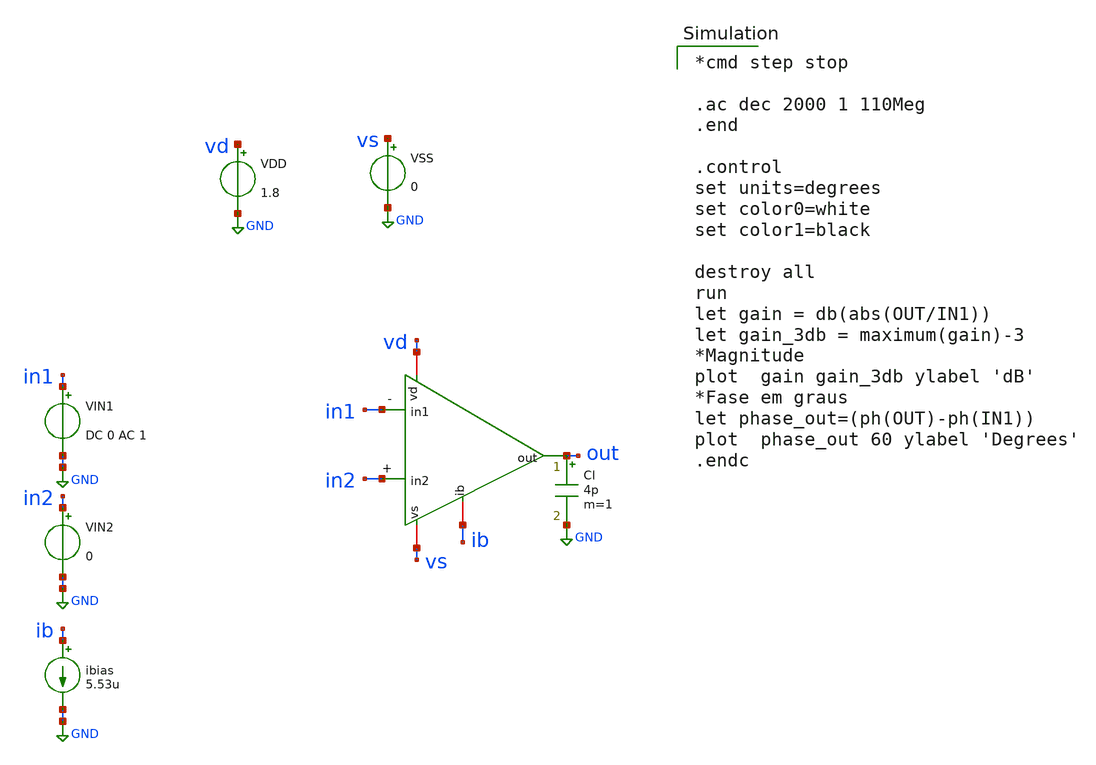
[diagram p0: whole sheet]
** sch_path: amp-op/xschem/ampop_tb-ac.sch
* Copyright 2020 Stefan Frederik Schippers
* Licensed under the Apache License, Version 2.0 (the "License");
* you may not use this file except in compliance with the License.
* You may obtain a copy of the License at
* https://www.apache.org/licenses/LICENSE-2.0
* Unless required by applicable law or agreed to in writing, software
* distributed under the License is distributed on an "AS IS" BASIS,
* WITHOUT WARRANTIES OR CONDITIONS OF ANY KIND, either express or implied.
* See the License for the specific language governing permissions and
* limitations under the License.
**.subckt ampop_tb-ac
VIN2 in2 GND 0
VIN1 in1 GND DC 0 AC 1
ibias ib GND 5.53u
VDD vd GND 1.8
VSS vs GND 0
Cl out GND 4p m=1
x1 vd in1 in2 out ib vs ampop
**** begin user architecture code

*cmd step stop

.ac dec 2000 1 110Meg
.end

.control
set units=degrees
set color0=white
set color1=black

destroy all
run
let gain = db(abs(OUT/IN1))
let gain_3db = maximum(gain)-3
*Magnitude
plot  gain gain_3db ylabel 'dB'
*Fase em graus
let phase_out=(ph(OUT)-ph(IN1))
plot  phase_out 60 ylabel 'Degrees'
.endc

 .lib $::SKYWATER_MODELS/sky130.lib.spice tt
.include $::SKYWATER_STDCELLS/sky130_fd_sc_hd.spice

**** end user architecture code
**.ends
.GLOBAL GND
.end
